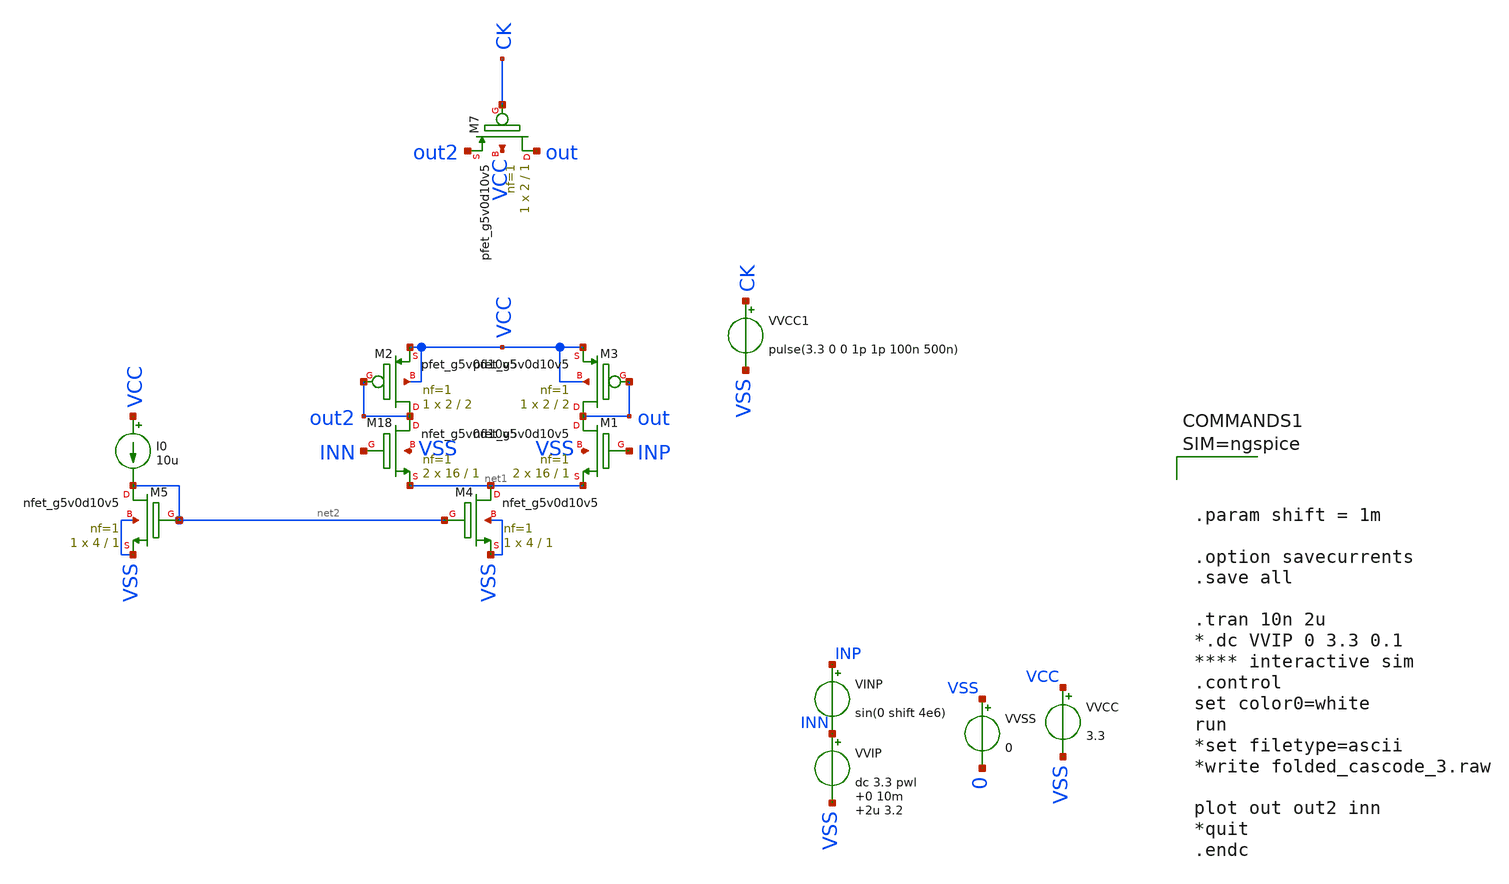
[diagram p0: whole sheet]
** sch_path: folded_cascode/folded_cascode_3.sch
.lib $::SKYWATER_MODELS/sky130.lib.spice.tt.red tt_mm
.include $::SKYWATER_STDCELLS/sky130_fd_sc_hd.spice

**.subckt folded_cascode_3
VINP INP INN sin(0 shift 4e6)
VVSS VSS 0 0
VVCC VCC VSS 3.3
VVIP INN VSS dc 3.3 pwl 0 10m 2u 3.2

XM18 out2 INN net1 VSS sky130_fd_pr__nfet_g5v0d10v5 L=1 W=16 nf=1 ad='int((nf+1)/2) * W/nf * 0.29' as='int((nf+2)/2) * W/nf * 0.29'
+ pd='2*int((nf+1)/2) * (W/nf + 0.29)' ps='2*int((nf+2)/2) * (W/nf + 0.29)' nrd='0.29 / W' nrs='0.29 / W'
+ sa=0 sb=0 sd=0 mult=2 m=2
XM1 out INP net1 VSS sky130_fd_pr__nfet_g5v0d10v5 L=1 W=16 nf=1 ad='int((nf+1)/2) * W/nf * 0.29' as='int((nf+2)/2) * W/nf * 0.29'
+ pd='2*int((nf+1)/2) * (W/nf + 0.29)' ps='2*int((nf+2)/2) * (W/nf + 0.29)' nrd='0.29 / W' nrs='0.29 / W'
+ sa=0 sb=0 sd=0 mult=2 m=2
XM2 out2 out2 VCC VCC sky130_fd_pr__pfet_g5v0d10v5 L=2 W=2 nf=1 ad='int((nf+1)/2) * W/nf * 0.29' as='int((nf+2)/2) * W/nf * 0.29'
+ pd='2*int((nf+1)/2) * (W/nf + 0.29)' ps='2*int((nf+2)/2) * (W/nf + 0.29)' nrd='0.29 / W' nrs='0.29 / W'
+ sa=0 sb=0 sd=0 mult=1 m=1
XM3 out out VCC VCC sky130_fd_pr__pfet_g5v0d10v5 L=2 W=2 nf=1 ad='int((nf+1)/2) * W/nf * 0.29' as='int((nf+2)/2) * W/nf * 0.29'
+ pd='2*int((nf+1)/2) * (W/nf + 0.29)' ps='2*int((nf+2)/2) * (W/nf + 0.29)' nrd='0.29 / W' nrs='0.29 / W'
+ sa=0 sb=0 sd=0 mult=1 m=1
XM4 net1 net2 VSS VSS sky130_fd_pr__nfet_g5v0d10v5 L=1 W=4 nf=1 ad='int((nf+1)/2) * W/nf * 0.29' as='int((nf+2)/2) * W/nf * 0.29'
+ pd='2*int((nf+1)/2) * (W/nf + 0.29)' ps='2*int((nf+2)/2) * (W/nf + 0.29)' nrd='0.29 / W' nrs='0.29 / W'
+ sa=0 sb=0 sd=0 mult=1 m=1
XM5 net2 net2 VSS VSS sky130_fd_pr__nfet_g5v0d10v5 L=1 W=4 nf=1 ad='int((nf+1)/2) * W/nf * 0.29' as='int((nf+2)/2) * W/nf * 0.29'
+ pd='2*int((nf+1)/2) * (W/nf + 0.29)' ps='2*int((nf+2)/2) * (W/nf + 0.29)' nrd='0.29 / W' nrs='0.29 / W'
+ sa=0 sb=0 sd=0 mult=1 m=1
I0 VCC net2 10u
XM7 out CK out2 VCC sky130_fd_pr__pfet_g5v0d10v5 L=1 W=2 nf=1 ad='int((nf+1)/2) * W/nf * 0.29' as='int((nf+2)/2) * W/nf * 0.29'
+ pd='2*int((nf+1)/2) * (W/nf + 0.29)' ps='2*int((nf+2)/2) * (W/nf + 0.29)' nrd='0.29 / W' nrs='0.29 / W'
+ sa=0 sb=0 sd=0 mult=1 m=1
VVCC1 CK VSS pulse(3.3 0 0 1p 1p 100n 500n)
**** begin user architecture code




.param shift = 1m

.option savecurrents
.save all

.tran 10n 2u
*.dc VVIP 0 3.3 0.1
**** interactive sim
.control
set color0=white
run
*set filetype=ascii
*write folded_cascode_3.raw

plot out out2 inn
*quit
.endc



**** end user architecture code
**.ends
.end
